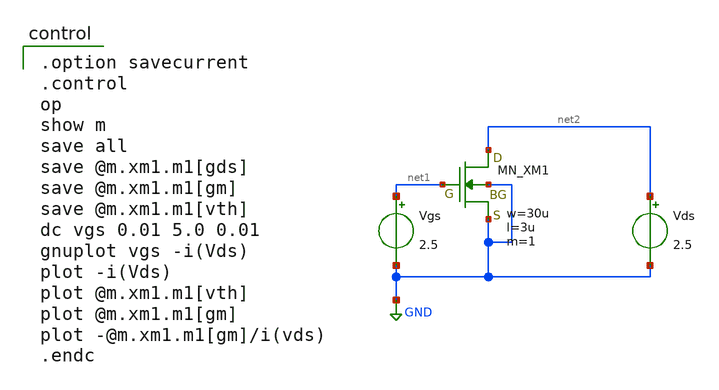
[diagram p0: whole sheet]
** sch_path: IO_202604/06/xschem/nfet_idvgs.sch
**.subckt nfet_idvgs
Vgs net1 GND 2.5
Vds net2 GND 2.5
XM1 net2 net1 GND GND NMOS w=30u l=3u as=0 ad=0 ps=0 pd=0 nrd=0 nrs=0 m=1
**** begin user architecture code

.option savecurrent
.control
op
show m
save all
save @m.xm1.m1[gds]
save @m.xm1.m1[gm]
save @m.xm1.m1[vth]
dc vgs 0.01 5.0 0.01
gnuplot vgs -i(Vds)
plot -i(Vds)
plot @m.xm1.m1[vth]
plot @m.xm1.m1[gm]
plot -@m.xm1.m1[gm]/i(vds)
.endc

 .include $::LIB/../ip62_models
**** end user architecture code
**.ends
.GLOBAL GND
.end
